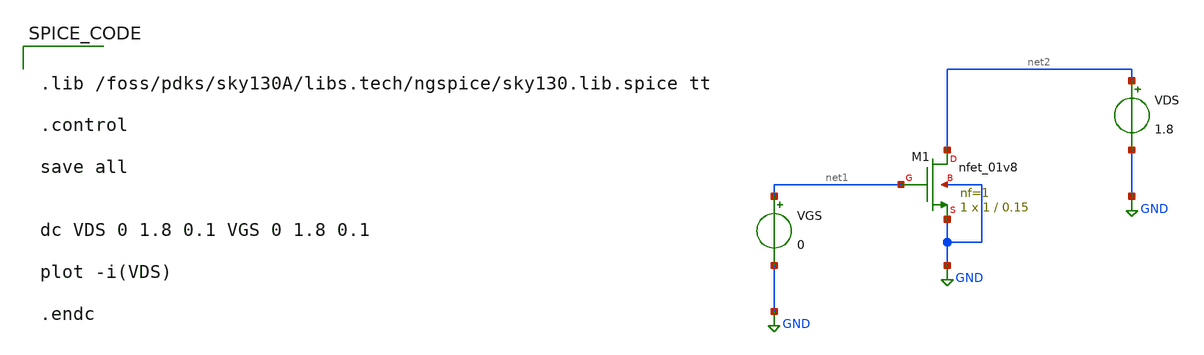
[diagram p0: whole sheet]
** sch_path: nmos_charac.sch
**.subckt nmos_charac
XM1 net2 net1 GND GND sky130_fd_pr__nfet_01v8 L=0.15 W=1 nf=1 ad='int((nf+1)/2) * W/nf * 0.29' as='int((nf+2)/2) * W/nf * 0.29'
+ pd='2*int((nf+1)/2) * (W/nf + 0.29)' ps='2*int((nf+2)/2) * (W/nf + 0.29)' nrd='0.29 / W' nrs='0.29 / W'
+ sa=0 sb=0 sd=0 mult=1 m=1
VGS net1 GND 0
VDS net2 GND 1.8
**** begin user architecture code


.lib /foss/pdks/sky130A/libs.tech/ngspice/sky130.lib.spice tt

.control

save all


dc VDS 0 1.8 0.1 VGS 0 1.8 0.1

plot -i(VDS)

.endc




**** end user architecture code
**.ends
.GLOBAL GND
.end
